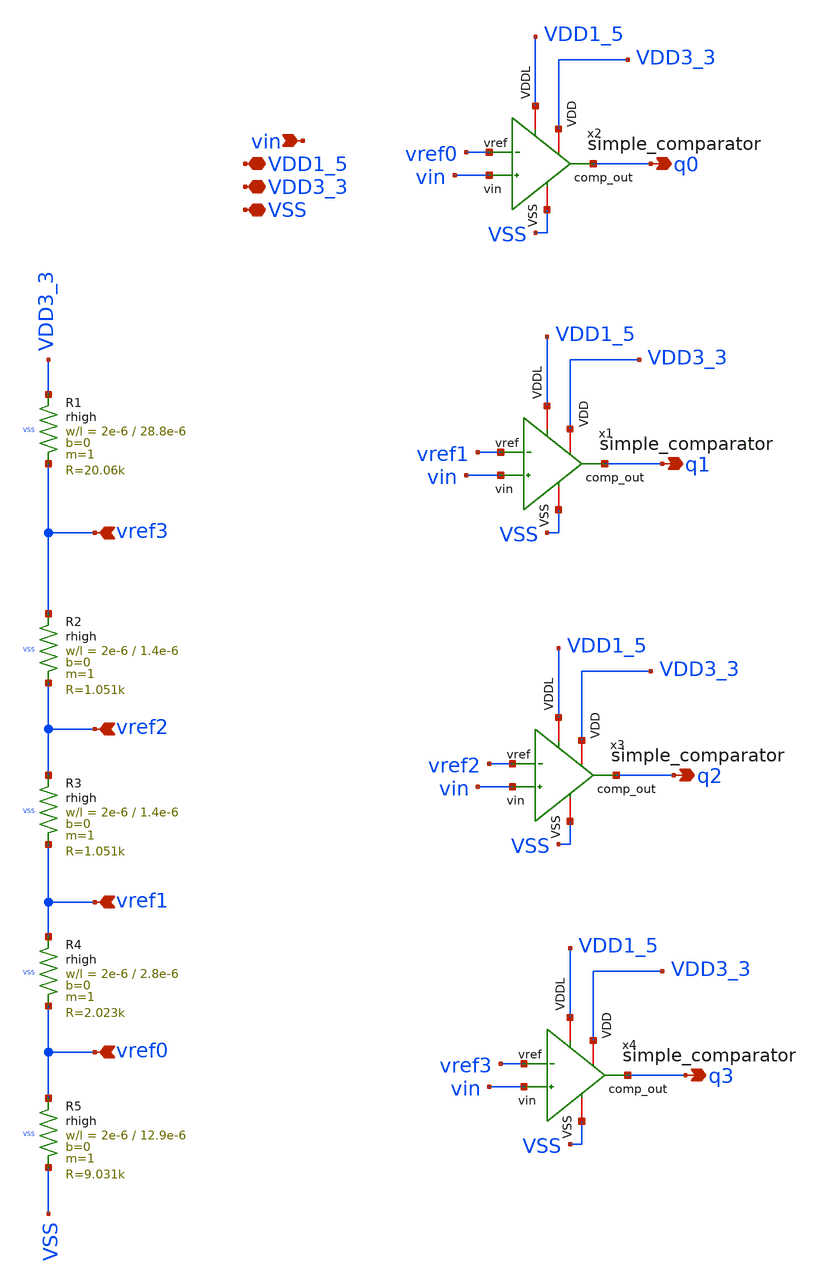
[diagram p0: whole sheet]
** sch_path: macros/heichips26_ook_top/macros/ook_analog_system/schematic/xschem/simple_comparator_stage.sch
**.subckt simple_comparator_stage VDD3_3 VSS VDD1_5 vin q0 vref3 vref2 vref1 vref0 q1 q2 q3
*.iopin VDD3_3
*.iopin VSS
*.iopin VDD1_5
*.ipin vin
*.opin q0
*.ipin vref3
*.ipin vref2
*.ipin vref1
*.ipin vref0
*.opin q1
*.opin q2
*.opin q3
x2 VDD1_5 VSS VDD3_3 vref0 vin q0 simple_comparator
XR1 VDD3_3 vref3 VSS rhigh w=2e-6 l=28.8e-6 m=1 b=0 mm_ok=1
XR5 vref0 VSS VSS rhigh w=2e-6 l=12.9e-6 m=1 b=0 mm_ok=1
x1 VDD1_5 VSS VDD3_3 vref1 vin q1 simple_comparator
x3 VDD1_5 VSS VDD3_3 vref2 vin q2 simple_comparator
x4 VDD1_5 VSS VDD3_3 vref3 vin q3 simple_comparator
XR4 vref1 vref0 VSS rhigh w=2e-6 l=2.8e-6 m=1 b=0 mm_ok=1
XR3 vref2 vref1 VSS rhigh w=2e-6 l=1.4e-6 m=1 b=0 mm_ok=1
XR2 vref3 vref2 VSS rhigh w=2e-6 l=1.4e-6 m=1 b=0 mm_ok=1
**.ends

* expanding   symbol:
*+  /home/belal/HeiChips/heichips26-on-off/macros/heichips26_ook_top/macros/ook_analog_system/schematic/xschem/simple_comparator.sym # of pins=6
** sym_path: macros/heichips26_ook_top/macros/ook_analog_system/schematic/xschem/simple_comparator.sym
** sch_path: macros/heichips26_ook_top/macros/ook_analog_system/schematic/xschem/simple_comparator.sch
.subckt simple_comparator VDDL VSS VDD vref vin comp_out
*.ipin vin
*.ipin vref
*.iopin VDD
*.iopin VSS
*.opin comp_out
*.iopin VDDL
XMBIAS vbias vbias VDD VDD sg13_hv_pmos w=4u l=0.5u ng=1 m=1 mm_ok=1
XRBIAS vbias VSS VSS rhigh w=2e-6 l=9.27e-6 m=1 b=15 ps=0.18e-6 mm_ok=1
XM3P net4 vbias VDD VDD sg13_hv_pmos w=4u l=0.5u ng=1 m=1 mm_ok=1
XM1P outn vin net4 VDD sg13_hv_pmos w=4u l=0.5u ng=1 m=4 mm_ok=1
XM2P net1 vref net4 VDD sg13_hv_pmos w=4u l=0.5u ng=1 m=4 mm_ok=1
XM4N outn outn VSS VSS sg13_hv_nmos w=2u l=0.5u ng=1 m=4 mm_ok=1
XM5N net1 outn VSS VSS sg13_hv_nmos w=2u l=0.5u ng=1 m=4 mm_ok=1
XMP1 net2 net1 VDD VDD sg13_hv_pmos w=8u l=0.45u ng=1 m=1 mm_ok=1
XMN1 net2 net1 VSS VSS sg13_hv_nmos w=4u l=0.45u ng=1 m=1 mm_ok=1
XMP2 comp_out net3 VDDL VDDL sg13_lv_pmos w=8u l=0.13u ng=1 m=1 mm_ok=1
XMBIAS1 vbias vbias vbias VDD sg13_hv_pmos w=4u l=0.5u ng=1 m=1 mm_ok=1
XMBIAS2 VDD VDD VDD VDD sg13_hv_pmos w=4u l=0.5u ng=1 m=1 mm_ok=1
XM1 VDD VDD VDD VDD sg13_hv_pmos w=4u l=0.5u ng=1 m=1 mm_ok=1
XM2 net4 net4 net4 VDD sg13_hv_pmos w=4u l=0.5u ng=1 m=1 mm_ok=1
XMP3 net2 net2 net2 VDD sg13_hv_pmos w=8u l=0.45u ng=1 m=1 mm_ok=1
XMP4 VDD VDD VDD VDD sg13_hv_pmos w=8u l=0.45u ng=1 m=1 mm_ok=1
XMP5 VDDL VDDL VDDL VDDL sg13_lv_pmos w=8u l=0.13u ng=1 m=1 mm_ok=1
XMP6 comp_out comp_out comp_out VDDL sg13_lv_pmos w=8u l=0.13u ng=1 m=1 mm_ok=1
XMN3 comp_out comp_out comp_out VSS sg13_lv_nmos w=4u l=0.13u ng=1 m=1 mm_ok=1
XMN4 VSS VSS VSS VSS sg13_lv_nmos w=4u l=0.13u ng=1 m=1 mm_ok=1
XMN5 net2 net2 net2 VSS sg13_hv_nmos w=4u l=0.45u ng=1 m=1 mm_ok=1
XMN6 VSS VSS VSS VSS sg13_hv_nmos w=4u l=0.45u ng=1 m=1 mm_ok=1
XM3 net4 net4 net4 VDD sg13_hv_pmos w=4u l=0.5u ng=1 m=1 mm_ok=1
XM4 outn outn outn VDD sg13_hv_pmos w=4u l=0.5u ng=1 m=1 mm_ok=1
XM5 net1 net1 net1 VSS sg13_hv_nmos w=2u l=0.5u ng=1 m=1 mm_ok=1
XM6 VSS VSS VSS VSS sg13_hv_nmos w=2u l=0.5u ng=1 m=1 mm_ok=1
XM7 net4 net4 net4 VDD sg13_hv_pmos w=4u l=0.5u ng=1 m=1 mm_ok=1
XM8 net1 net1 net1 VDD sg13_hv_pmos w=4u l=0.5u ng=1 m=1 mm_ok=1
XM9 outn outn outn VSS sg13_hv_nmos w=2u l=0.5u ng=1 m=1 mm_ok=1
XM10 VSS VSS VSS VSS sg13_hv_nmos w=2u l=0.5u ng=1 m=1 mm_ok=1
XMN8 comp_out net3 VSS VSS sg13_lv_nmos w=4u l=0.13u ng=1 m=1 mm_ok=1
XMP7 net3 net2 VDDL VDDL sg13_hv_pmos w=8u l=0.45u ng=1 m=1 mm_ok=1
XMN2 net3 net2 VSS VSS sg13_hv_nmos w=4u l=0.45u ng=1 m=1 mm_ok=1
XMP8 net3 net3 net3 VDDL sg13_hv_pmos w=8u l=0.45u ng=1 m=1 mm_ok=1
XMP9 VDDL VDDL VDDL VDDL sg13_hv_pmos w=8u l=0.45u ng=1 m=1 mm_ok=1
XMN7 net3 net3 net3 VSS sg13_hv_nmos w=4u l=0.45u ng=1 m=1 mm_ok=1
XMN9 VSS VSS VSS VSS sg13_hv_nmos w=4u l=0.45u ng=1 m=1 mm_ok=1
.ends

.end
